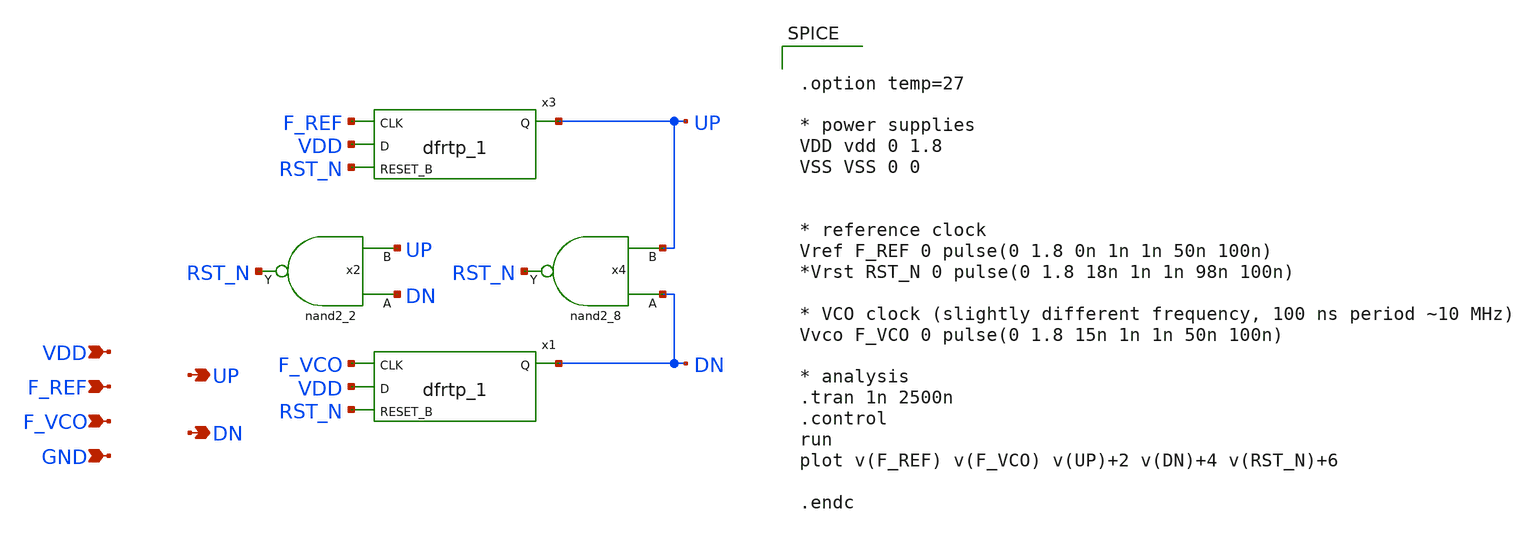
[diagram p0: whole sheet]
** sch_path: src/PFD_std.sch
**.subckt PFD_std UP F_REF VDD GND DN F_VCO
*.opin UP
*.ipin F_REF
*.ipin VDD
*.ipin GND
*.opin DN
*.ipin F_VCO
x1 F_VCO VDD RST_N GND GND VDD VDD DN sky130_fd_sc_hd__dfrtp_1
x2 DN UP GND GND VDD VDD RST_N sky130_fd_sc_hd__nand2_2
x4 DN UP GND GND VDD VDD RST_N sky130_fd_sc_hd__nand2_8
x3 F_REF VDD RST_N GND GND VDD VDD UP sky130_fd_sc_hd__dfrtp_1
**** begin user architecture code

** opencircuitdesign pdks install
.lib $::SKYWATER_MODELS/sky130.lib.spice tt
.include /foss/pdks/ciel/sky130/versions/8afc8346a57fe1ab7934ba5a6056ea8b43078e71/sky130A/libs.ref/sky130_fd_sc_hd/spice/sky130_fd_sc_hd.spice
.global VDD GND




.option temp=27

* power supplies
VDD vdd 0 1.8
VSS VSS 0 0


* reference clock
Vref F_REF 0 pulse(0 1.8 0n 1n 1n 50n 100n)
*Vrst RST_N 0 pulse(0 1.8 18n 1n 1n 98n 100n)

* VCO clock (slightly different frequency, 100 ns period ~10 MHz)
Vvco F_VCO 0 pulse(0 1.8 15n 1n 1n 50n 100n)

* analysis
.tran 1n 2500n
.control
run
plot v(F_REF) v(F_VCO) v(UP)+2 v(DN)+4 v(RST_N)+6

.endc


**** end user architecture code
**.ends
.end
